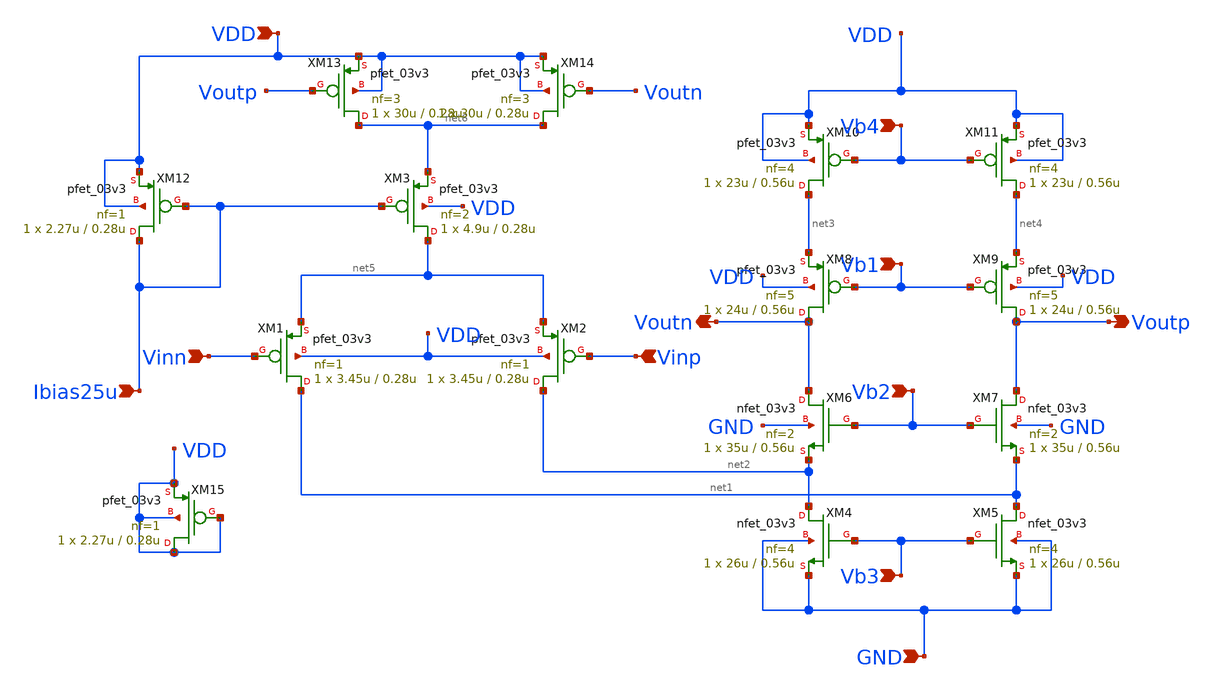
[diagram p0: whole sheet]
** sch_path: jz_fda2/xschem/foldedcasc_cmfb_forlayout_new.sch
**.subckt foldedcasc_cmfb_forlayout_new VDD Voutp Vinn Ibias25u GND Vinp Voutn Vb4 Vb1 Vb2 Vb3
*.ipin VDD
*.opin Voutp
*.ipin Vinn
*.ipin Ibias25u
*.ipin GND
*.ipin Vinp
*.opin Voutn
*.ipin Vb4
*.ipin Vb1
*.ipin Vb2
*.ipin Vb3
XM5 net1 Vb3 GND GND nfet_03v3 L=0.56u W=26u nf=4 ad='int((nf+1)/2) * W/nf * 0.18u' as='int((nf+2)/2) * W/nf * 0.18u'
+ pd='2*int((nf+1)/2) * (W/nf + 0.18u)' ps='2*int((nf+2)/2) * (W/nf + 0.18u)' nrd='0.18u / W' nrs='0.18u / W'
+ sa=0 sb=0 sd=0 m=1
XM6 Voutn Vb2 net2 GND nfet_03v3 L=0.56u W=35u nf=2 ad='int((nf+1)/2) * W/nf * 0.18u' as='int((nf+2)/2) * W/nf * 0.18u'
+ pd='2*int((nf+1)/2) * (W/nf + 0.18u)' ps='2*int((nf+2)/2) * (W/nf + 0.18u)' nrd='0.18u / W' nrs='0.18u / W'
+ sa=0 sb=0 sd=0 m=1
XM7 Voutp Vb2 net1 GND nfet_03v3 L=0.56u W=35u nf=2 ad='int((nf+1)/2) * W/nf * 0.18u' as='int((nf+2)/2) * W/nf * 0.18u'
+ pd='2*int((nf+1)/2) * (W/nf + 0.18u)' ps='2*int((nf+2)/2) * (W/nf + 0.18u)' nrd='0.18u / W' nrs='0.18u / W'
+ sa=0 sb=0 sd=0 m=1
XM8 Voutn Vb1 net3 VDD pfet_03v3 L=0.56u W=24u nf=5 ad='int((nf+1)/2) * W/nf * 0.18u' as='int((nf+2)/2) * W/nf * 0.18u'
+ pd='2*int((nf+1)/2) * (W/nf + 0.18u)' ps='2*int((nf+2)/2) * (W/nf + 0.18u)' nrd='0.18u / W' nrs='0.18u / W'
+ sa=0 sb=0 sd=0 m=1
XM9 Voutp Vb1 net4 VDD pfet_03v3 L=0.56u W=24u nf=5 ad='int((nf+1)/2) * W/nf * 0.18u' as='int((nf+2)/2) * W/nf * 0.18u'
+ pd='2*int((nf+1)/2) * (W/nf + 0.18u)' ps='2*int((nf+2)/2) * (W/nf + 0.18u)' nrd='0.18u / W' nrs='0.18u / W'
+ sa=0 sb=0 sd=0 m=1
XM10 net3 Vb4 VDD VDD pfet_03v3 L=0.56u W=23u nf=4 ad='int((nf+1)/2) * W/nf * 0.18u' as='int((nf+2)/2) * W/nf * 0.18u'
+ pd='2*int((nf+1)/2) * (W/nf + 0.18u)' ps='2*int((nf+2)/2) * (W/nf + 0.18u)' nrd='0.18u / W' nrs='0.18u / W'
+ sa=0 sb=0 sd=0 m=1
XM11 net4 Vb4 VDD VDD pfet_03v3 L=0.56u W=23u nf=4 ad='int((nf+1)/2) * W/nf * 0.18u' as='int((nf+2)/2) * W/nf * 0.18u'
+ pd='2*int((nf+1)/2) * (W/nf + 0.18u)' ps='2*int((nf+2)/2) * (W/nf + 0.18u)' nrd='0.18u / W' nrs='0.18u / W'
+ sa=0 sb=0 sd=0 m=1
XM1 net1 Vinn net5 VDD pfet_03v3 L=0.28u W=3.45u nf=1 ad='int((nf+1)/2) * W/nf * 0.18u' as='int((nf+2)/2) * W/nf * 0.18u'
+ pd='2*int((nf+1)/2) * (W/nf + 0.18u)' ps='2*int((nf+2)/2) * (W/nf + 0.18u)' nrd='0.18u / W' nrs='0.18u / W'
+ sa=0 sb=0 sd=0 m=1
XM2 net2 Vinp net5 VDD pfet_03v3 L=0.28u W=3.45u nf=1 ad='int((nf+1)/2) * W/nf * 0.18u' as='int((nf+2)/2) * W/nf * 0.18u'
+ pd='2*int((nf+1)/2) * (W/nf + 0.18u)' ps='2*int((nf+2)/2) * (W/nf + 0.18u)' nrd='0.18u / W' nrs='0.18u / W'
+ sa=0 sb=0 sd=0 m=1
XM3 net5 Ibias25u net6 VDD pfet_03v3 L=0.28u W=4.9u nf=2 ad='int((nf+1)/2) * W/nf * 0.18u' as='int((nf+2)/2) * W/nf * 0.18u'
+ pd='2*int((nf+1)/2) * (W/nf + 0.18u)' ps='2*int((nf+2)/2) * (W/nf + 0.18u)' nrd='0.18u / W' nrs='0.18u / W'
+ sa=0 sb=0 sd=0 m=1
XM12 Ibias25u Ibias25u VDD VDD pfet_03v3 L=0.28u W=2.27u nf=1 ad='int((nf+1)/2) * W/nf * 0.18u' as='int((nf+2)/2) * W/nf * 0.18u'
+ pd='2*int((nf+1)/2) * (W/nf + 0.18u)' ps='2*int((nf+2)/2) * (W/nf + 0.18u)' nrd='0.18u / W' nrs='0.18u / W'
+ sa=0 sb=0 sd=0 m=1
XM13 net6 Voutp VDD VDD pfet_03v3 L=0.28u W=30u nf=3 ad='int((nf+1)/2) * W/nf * 0.18u' as='int((nf+2)/2) * W/nf * 0.18u'
+ pd='2*int((nf+1)/2) * (W/nf + 0.18u)' ps='2*int((nf+2)/2) * (W/nf + 0.18u)' nrd='0.18u / W' nrs='0.18u / W'
+ sa=0 sb=0 sd=0 m=1
XM14 net6 Voutn VDD VDD pfet_03v3 L=0.28u W=30u nf=3 ad='int((nf+1)/2) * W/nf * 0.18u' as='int((nf+2)/2) * W/nf * 0.18u'
+ pd='2*int((nf+1)/2) * (W/nf + 0.18u)' ps='2*int((nf+2)/2) * (W/nf + 0.18u)' nrd='0.18u / W' nrs='0.18u / W'
+ sa=0 sb=0 sd=0 m=1
XM4 net2 Vb3 GND GND nfet_03v3 L=0.56u W=26u nf=4 ad='int((nf+1)/2) * W/nf * 0.18u' as='int((nf+2)/2) * W/nf * 0.18u'
+ pd='2*int((nf+1)/2) * (W/nf + 0.18u)' ps='2*int((nf+2)/2) * (W/nf + 0.18u)' nrd='0.18u / W' nrs='0.18u / W'
+ sa=0 sb=0 sd=0 m=1
XM15 VDD VDD VDD VDD pfet_03v3 L=0.28u W=2.27u nf=1 ad='int((nf+1)/2) * W/nf * 0.18u' as='int((nf+2)/2) * W/nf * 0.18u'
+ pd='2*int((nf+1)/2) * (W/nf + 0.18u)' ps='2*int((nf+2)/2) * (W/nf + 0.18u)' nrd='0.18u / W' nrs='0.18u / W'
+ sa=0 sb=0 sd=0 m=1
**.ends
.end
